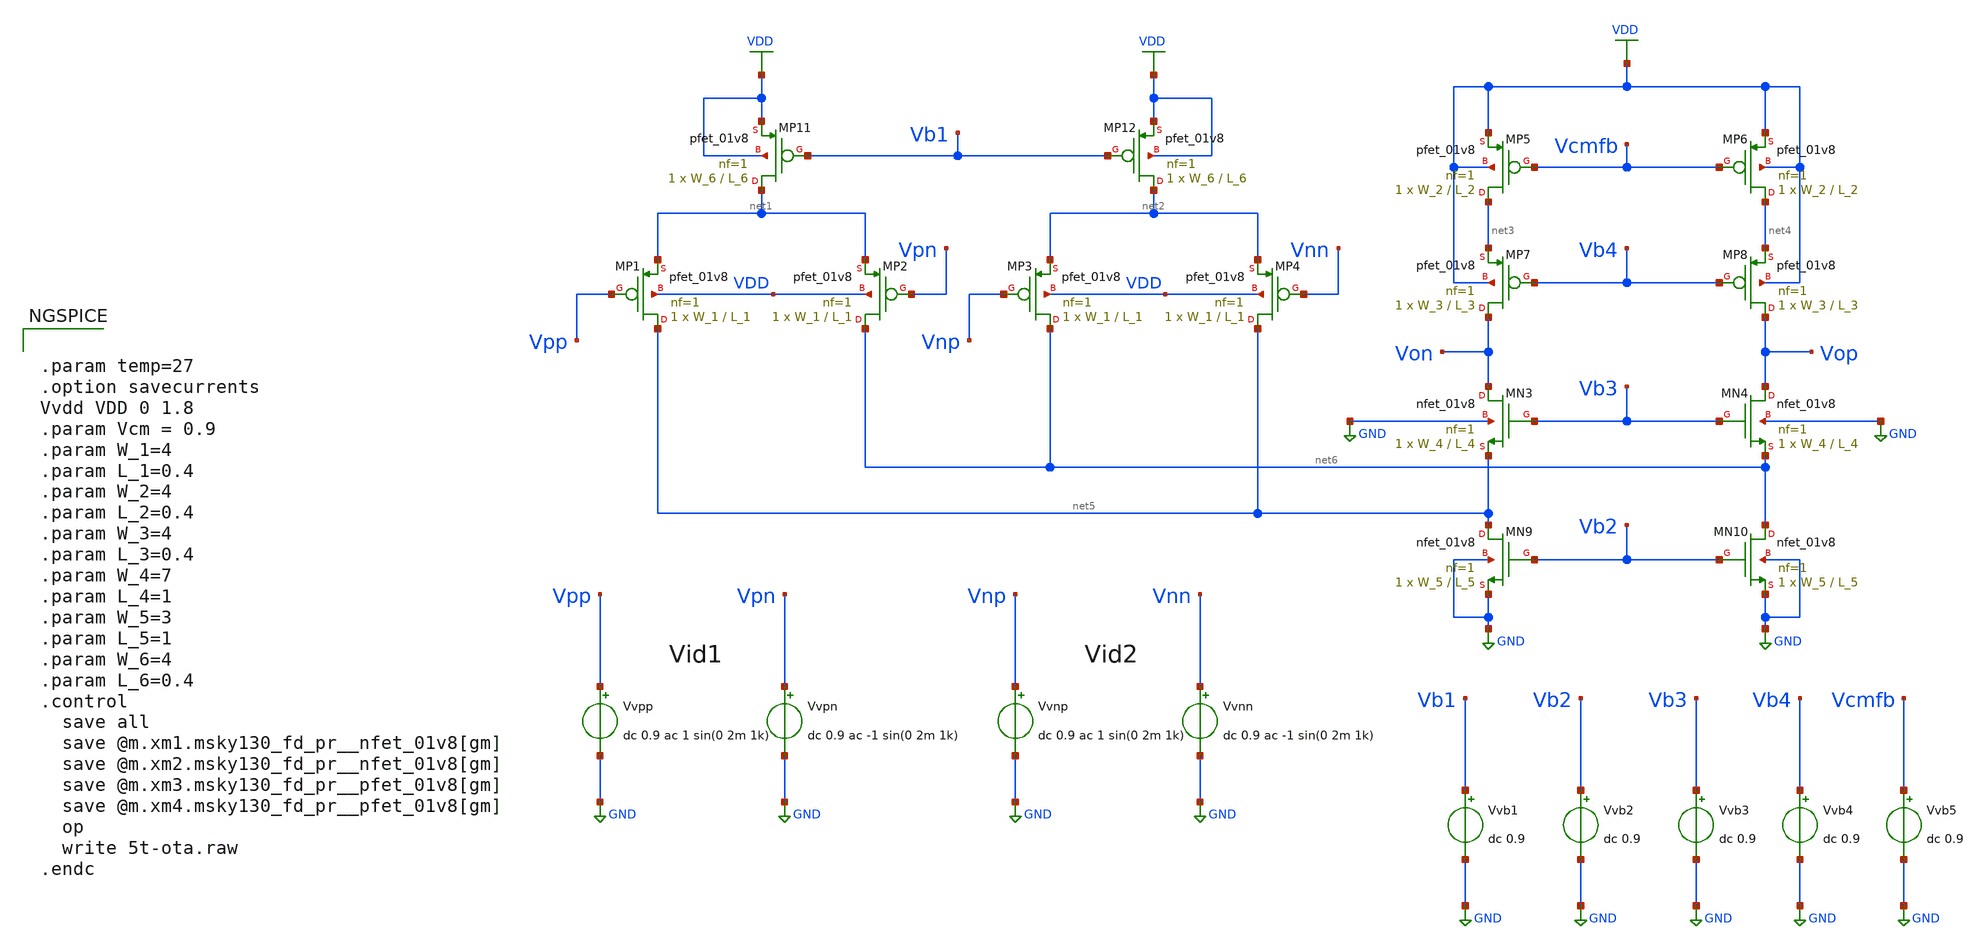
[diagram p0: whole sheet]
** sch_path: Xschem Simulations/FDDA/FDDA.sch
**.subckt FDDA
XMP1 net5 Vpp net1 VDD sky130_fd_pr__pfet_01v8 L=L_1 W=W_1 nf=1 ad='int((1 + 1)/2) * W_1 / 1 * 0.29'
+ as='int((1 + 2)/2) * W_1 / 1 * 0.29' pd='2*int((1 + 1)/2) * (W_1 / 1 + 0.29)' ps='2*int((1 + 2)/2) * (W_1 / 1 + 0.29)'
+ nrd='0.29 / W_1 ' nrs='0.29 / W_1 ' sa=0 sb=0 sd=0 mult=1 m=1
XMP2 net6 Vpn net1 VDD sky130_fd_pr__pfet_01v8 L=L_1 W=W_1 nf=1 ad='int((1 + 1)/2) * W_1 / 1 * 0.29'
+ as='int((1 + 2)/2) * W_1 / 1 * 0.29' pd='2*int((1 + 1)/2) * (W_1 / 1 + 0.29)' ps='2*int((1 + 2)/2) * (W_1 / 1 + 0.29)'
+ nrd='0.29 / W_1 ' nrs='0.29 / W_1 ' sa=0 sb=0 sd=0 mult=1 m=1
XMP3 net6 Vnp net2 VDD sky130_fd_pr__pfet_01v8 L=L_1 W=W_1 nf=1 ad='int((1 + 1)/2) * W_1 / 1 * 0.29'
+ as='int((1 + 2)/2) * W_1 / 1 * 0.29' pd='2*int((1 + 1)/2) * (W_1 / 1 + 0.29)' ps='2*int((1 + 2)/2) * (W_1 / 1 + 0.29)'
+ nrd='0.29 / W_1 ' nrs='0.29 / W_1 ' sa=0 sb=0 sd=0 mult=1 m=1
XMP4 net5 Vnn net2 VDD sky130_fd_pr__pfet_01v8 L=L_1 W=W_1 nf=1 ad='int((1 + 1)/2) * W_1 / 1 * 0.29'
+ as='int((1 + 2)/2) * W_1 / 1 * 0.29' pd='2*int((1 + 1)/2) * (W_1 / 1 + 0.29)' ps='2*int((1 + 2)/2) * (W_1 / 1 + 0.29)'
+ nrd='0.29 / W_1 ' nrs='0.29 / W_1 ' sa=0 sb=0 sd=0 mult=1 m=1
XMP5 net3 Vcmfb VDD VDD sky130_fd_pr__pfet_01v8 L=L_2 W=W_2 nf=1 ad='int((1 + 1)/2) * W_2 / 1 * 0.29'
+ as='int((1 + 2)/2) * W_2 / 1 * 0.29' pd='2*int((1 + 1)/2) * (W_2 / 1 + 0.29)' ps='2*int((1 + 2)/2) * (W_2 / 1 + 0.29)'
+ nrd='0.29 / W_2 ' nrs='0.29 / W_2 ' sa=0 sb=0 sd=0 mult=1 m=1
XMP6 net4 Vcmfb VDD VDD sky130_fd_pr__pfet_01v8 L=L_2 W=W_2 nf=1 ad='int((1 + 1)/2) * W_2 / 1 * 0.29'
+ as='int((1 + 2)/2) * W_2 / 1 * 0.29' pd='2*int((1 + 1)/2) * (W_2 / 1 + 0.29)' ps='2*int((1 + 2)/2) * (W_2 / 1 + 0.29)'
+ nrd='0.29 / W_2 ' nrs='0.29 / W_2 ' sa=0 sb=0 sd=0 mult=1 m=1
XMP7 Von Vb4 net3 VDD sky130_fd_pr__pfet_01v8 L=L_3 W=W_3 nf=1 ad='int((1 + 1)/2) * W_3 / 1 * 0.29' as='int((1 + 2)/2) * W_3 / 1 * 0.29'
+ pd='2*int((1 + 1)/2) * (W_3 / 1 + 0.29)' ps='2*int((1 + 2)/2) * (W_3 / 1 + 0.29)' nrd='0.29 / W_3 ' nrs='0.29 / W_3 '
+ sa=0 sb=0 sd=0 mult=1 m=1
XMP8 Vop Vb4 net4 VDD sky130_fd_pr__pfet_01v8 L=L_3 W=W_3 nf=1 ad='int((1 + 1)/2) * W_3 / 1 * 0.29' as='int((1 + 2)/2) * W_3 / 1 * 0.29'
+ pd='2*int((1 + 1)/2) * (W_3 / 1 + 0.29)' ps='2*int((1 + 2)/2) * (W_3 / 1 + 0.29)' nrd='0.29 / W_3 ' nrs='0.29 / W_3 '
+ sa=0 sb=0 sd=0 mult=1 m=1
XMP11 net1 Vb1 VDD VDD sky130_fd_pr__pfet_01v8 L=L_6 W=W_6 nf=1 ad='int((1 + 1)/2) * W_6 / 1 * 0.29'
+ as='int((1 + 2)/2) * W_6 / 1 * 0.29' pd='2*int((1 + 1)/2) * (W_6 / 1 + 0.29)' ps='2*int((1 + 2)/2) * (W_6 / 1 + 0.29)'
+ nrd='0.29 / W_6 ' nrs='0.29 / W_6 ' sa=0 sb=0 sd=0 mult=1 m=1
XMP12 net2 Vb1 VDD VDD sky130_fd_pr__pfet_01v8 L=L_6 W=W_6 nf=1 ad='int((1 + 1)/2) * W_6 / 1 * 0.29'
+ as='int((1 + 2)/2) * W_6 / 1 * 0.29' pd='2*int((1 + 1)/2) * (W_6 / 1 + 0.29)' ps='2*int((1 + 2)/2) * (W_6 / 1 + 0.29)'
+ nrd='0.29 / W_6 ' nrs='0.29 / W_6 ' sa=0 sb=0 sd=0 mult=1 m=1
XMN3 Von Vb3 net5 GND sky130_fd_pr__nfet_01v8 L=L_4 W=W_4 nf=1 ad='int((1 + 1)/2) * W_4 / 1 * 0.29' as='int((1 + 2)/2) * W_4 / 1 * 0.29'
+ pd='2*int((1 + 1)/2) * (W_4 / 1 + 0.29)' ps='2*int((1 + 2)/2) * (W_4 / 1 + 0.29)' nrd='0.29 / W_4 ' nrs='0.29 / W_4 '
+ sa=0 sb=0 sd=0 mult=1 m=1
XMN4 Vop Vb3 net6 GND sky130_fd_pr__nfet_01v8 L=L_4 W=W_4 nf=1 ad='int((1 + 1)/2) * W_4 / 1 * 0.29' as='int((1 + 2)/2) * W_4 / 1 * 0.29'
+ pd='2*int((1 + 1)/2) * (W_4 / 1 + 0.29)' ps='2*int((1 + 2)/2) * (W_4 / 1 + 0.29)' nrd='0.29 / W_4 ' nrs='0.29 / W_4 '
+ sa=0 sb=0 sd=0 mult=1 m=1
XMN9 net5 Vb2 GND GND sky130_fd_pr__nfet_01v8 L=L_5 W=W_5 nf=1 ad='int((1 + 1)/2) * W_5 / 1 * 0.29' as='int((1 + 2)/2) * W_5 / 1 * 0.29'
+ pd='2*int((1 + 1)/2) * (W_5 / 1 + 0.29)' ps='2*int((1 + 2)/2) * (W_5 / 1 + 0.29)' nrd='0.29 / W_5 ' nrs='0.29 / W_5 '
+ sa=0 sb=0 sd=0 mult=1 m=1
XMN10 net6 Vb2 GND GND sky130_fd_pr__nfet_01v8 L=L_5 W=W_5 nf=1 ad='int((1 + 1)/2) * W_5 / 1 * 0.29'
+ as='int((1 + 2)/2) * W_5 / 1 * 0.29' pd='2*int((1 + 1)/2) * (W_5 / 1 + 0.29)' ps='2*int((1 + 2)/2) * (W_5 / 1 + 0.29)'
+ nrd='0.29 / W_5 ' nrs='0.29 / W_5 ' sa=0 sb=0 sd=0 mult=1 m=1
Vvpp Vpp GND dc 0.9 ac 1 sin(0 2m 1k)
Vvpn Vpn GND dc 0.9 ac -1 sin(0 2m 1k)
Vvnp Vnp GND dc 0.9 ac 1 sin(0 2m 1k)
Vvnn Vnn GND dc 0.9 ac -1 sin(0 2m 1k)
Vvb1 Vb1 GND dc 0.9
Vvb2 Vb2 GND dc 0.9
Vvb3 Vb3 GND dc 0.9
Vvb4 Vb4 GND dc 0.9
Vvb5 Vcmfb GND dc 0.9
**** begin user architecture code

** opencircuitdesign pdks install
.lib $::SKYWATER_MODELS/sky130.lib.spice tt



.param temp=27
.option savecurrents
Vvdd VDD 0 1.8
.param Vcm = 0.9
.param W_1=4
.param L_1=0.4
.param W_2=4
.param L_2=0.4
.param W_3=4
.param L_3=0.4
.param W_4=7
.param L_4=1
.param W_5=3
.param L_5=1
.param W_6=4
.param L_6=0.4
.control
  save all
  save @m.xm1.msky130_fd_pr__nfet_01v8[gm]
  save @m.xm2.msky130_fd_pr__nfet_01v8[gm]
  save @m.xm3.msky130_fd_pr__pfet_01v8[gm]
  save @m.xm4.msky130_fd_pr__pfet_01v8[gm]
  op
  write 5t-ota.raw
.endc


**** end user architecture code
**.ends
.GLOBAL VDD
.GLOBAL GND
.end
